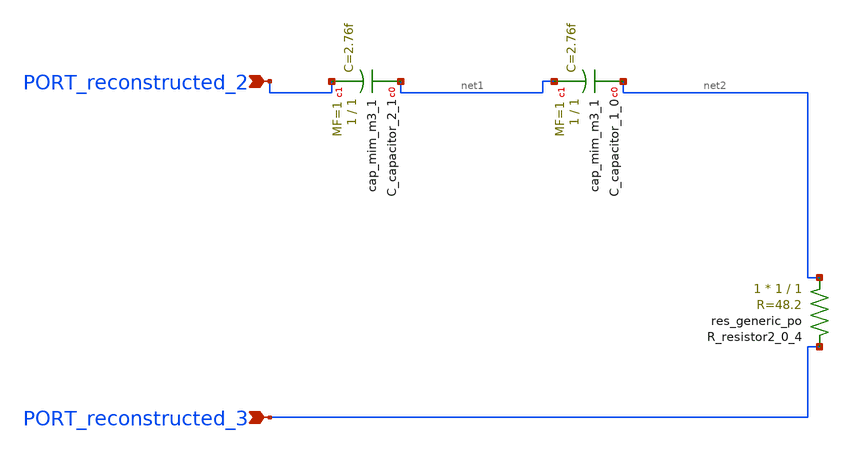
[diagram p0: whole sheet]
** sch_path: schematics/AMSNet/373.sch
**.subckt 373 PORT_reconstructed_2 PORT_reconstructed_3
*.ipin PORT_reconstructed_2
*.ipin PORT_reconstructed_3
XC_capacitor_1_0 net2 net1 sky130_fd_pr__cap_mim_m3_1 W=1 L=1 MF=1 m=1
XC_capacitor_2_1 net1 PORT_reconstructed_2 sky130_fd_pr__cap_mim_m3_1 W=1 L=1 MF=1 m=1
XR_resistor2_0_4 net2 PORT_reconstructed_3 sky130_fd_pr__res_generic_po W=1 L=1 m=1
**.ends
.end
